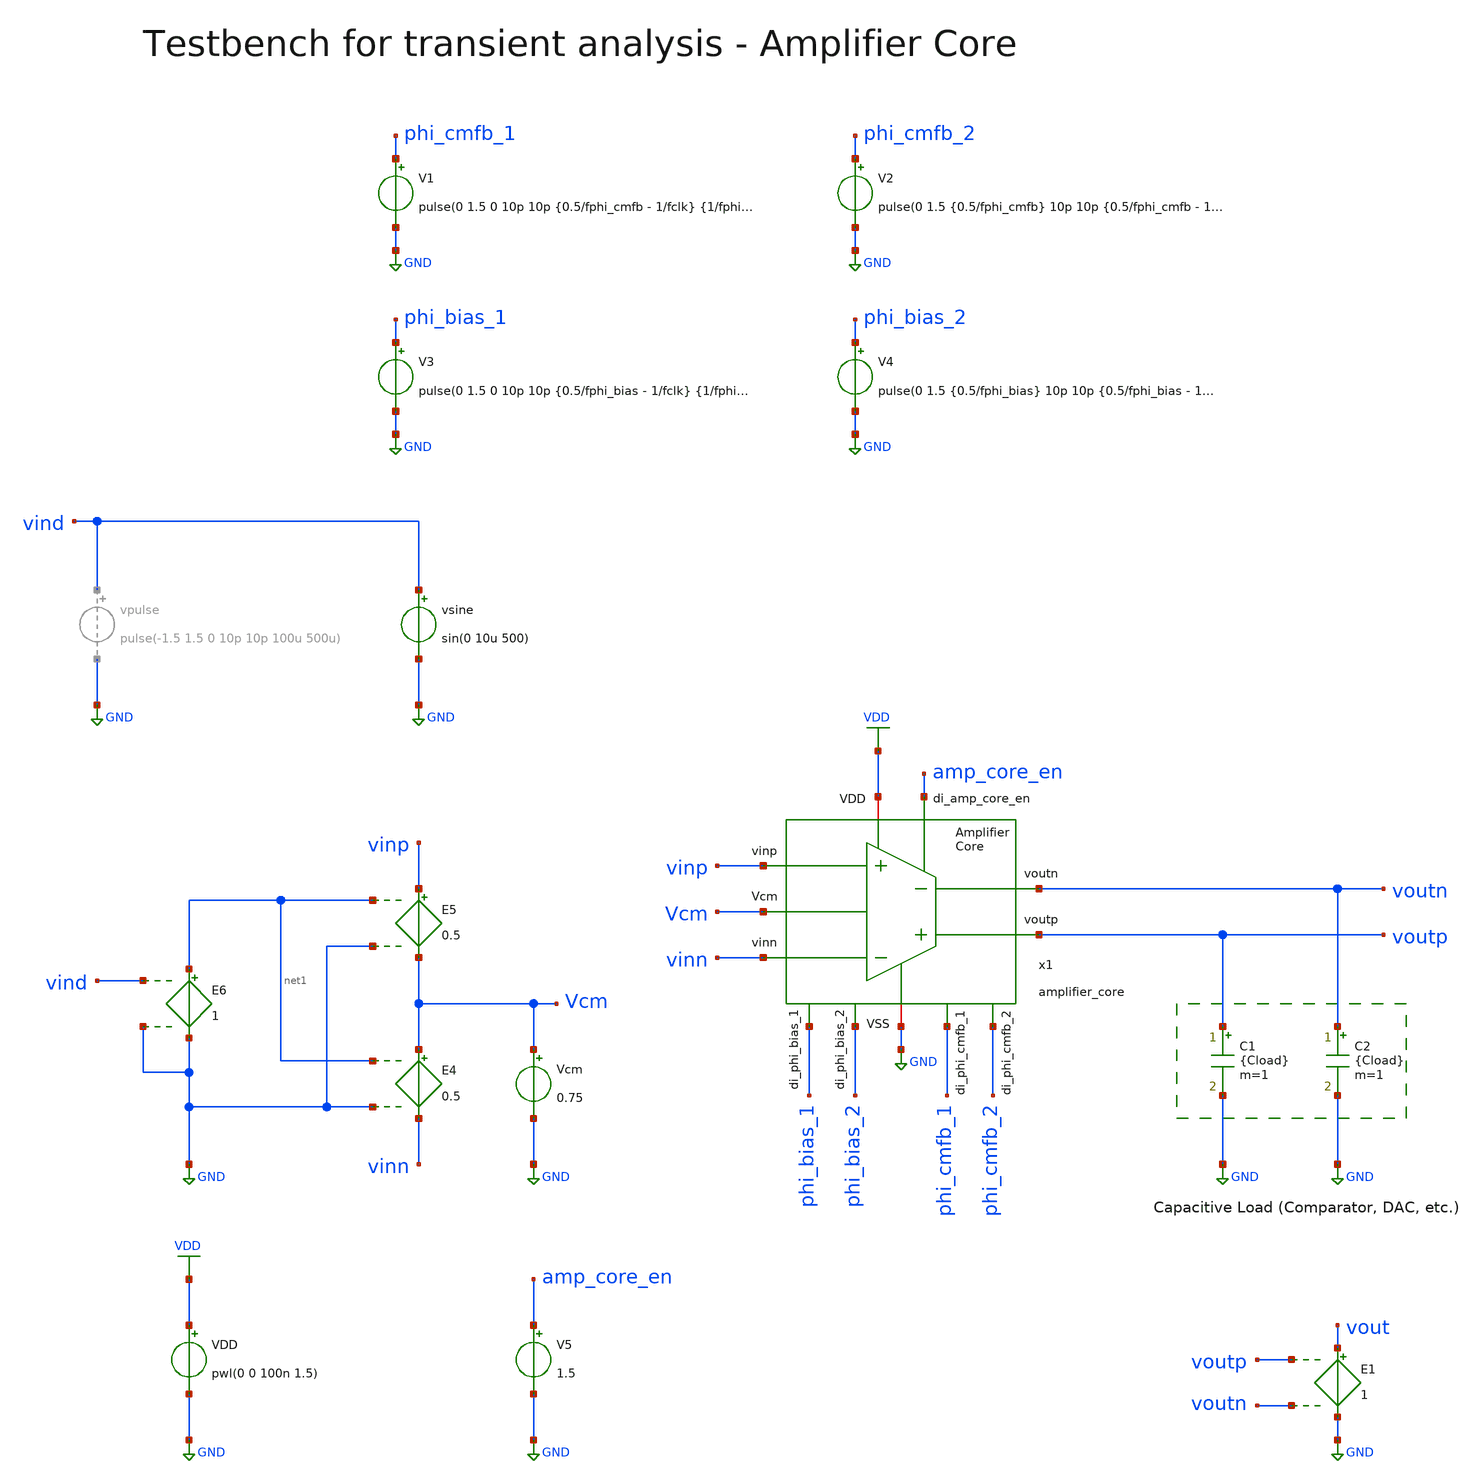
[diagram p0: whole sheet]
** sch_path: SG13G2_ATBS-ADC-main/xschem/bio_amplifier/amplifier_core/testbenches/amplifier_core_tb_tran.sch
**.subckt amplifier_core_tb_tran
C1 voutp GND {Cload} m=1
C2 voutn GND {Cload} m=1
Vcm Vcm GND 0.75
E4 Vcm vinn net1 GND 0.5
E5 vinp Vcm net1 GND 0.5
E6 net1 GND vind GND 1
V5 amp_core_en GND 1.5
vsine vind GND sin(0 10u 500)
x1 phi_cmfb_1 phi_bias_2 phi_bias_1 phi_cmfb_2 voutp voutn amp_core_en vinn vinp VDD GND Vcm
+ amplifier_core
V1 phi_cmfb_1 GND pulse(0 1.5 0 10p 10p {0.5/fphi_cmfb - 1/fclk} {1/fphi_cmfb})
V2 phi_cmfb_2 GND pulse(0 1.5 {0.5/fphi_cmfb} 10p 10p {0.5/fphi_cmfb - 1/fclk} {1/fphi_cmfb})
V3 phi_bias_1 GND pulse(0 1.5 0 10p 10p {0.5/fphi_bias - 1/fclk} {1/fphi_bias})
V4 phi_bias_2 GND pulse(0 1.5 {0.5/fphi_bias} 10p 10p {0.5/fphi_bias - 1/fclk} {1/fphi_bias})
E1 vout GND voutp voutn 1
VDD VDD GND pwl(0 0 100n 1.5)
**** begin user architecture code

.lib cornerMOSlv.lib mos_tt
.lib cornerMOShv.lib mos_tt
.lib cornerRES.lib res_typ



.param temp=27
.param fclk=8000000
.csparam fclk=fclk
.param fphi_cmfb=62500
.param fphi_bias=62500
* 228fF DAC + (1 - beta) * 3.3pF
.param Cload=3.49p

.options reltol=1e-2 abstol=1e-15 gmin=1e-15 rshunt=1e15
.control

* Turn on save all only for VDD current
* save all
save vind vinp vinn voutp voutn vout v(x1.Vbias) v(x1.Vbiasc)

* User Constants
let tstep = 1/fclk
* Sine
let tstop = 4m
* Pulse
* let tstop = 200u

* Operating Point Analysis
op
remzerovec
write amplifier_core_tb_tran.raw
set appendwrite

* Transient Analysis
tran $&tstep $&tstop
write amplifier_core_tb_tran.raw

* Plotting
plot vind
plot vinp vinn
plot vout
plot voutp voutn
plot v(x1.Vbias) v(x1.Vbiasc)
* plot i(VDD)

* Write Data
set wr_vecnames
set wr_singlescale
let Vbias=x1.Vbias
let Vbiasc=x1.Vbiasc
wrdata /foss/designs/SG13G2_ATBS-ADC-main/python/plot_simulations/data/amplifier_core_tb_tran.txt
+ v(vind) v(vinp) v(vinn) v(voutp) v(voutn) v(vout) v(Vbias) v(Vbiasc)

* quit
.endc


**** end user architecture code
**.ends
.GLOBAL GND
.GLOBAL VDD
.end
